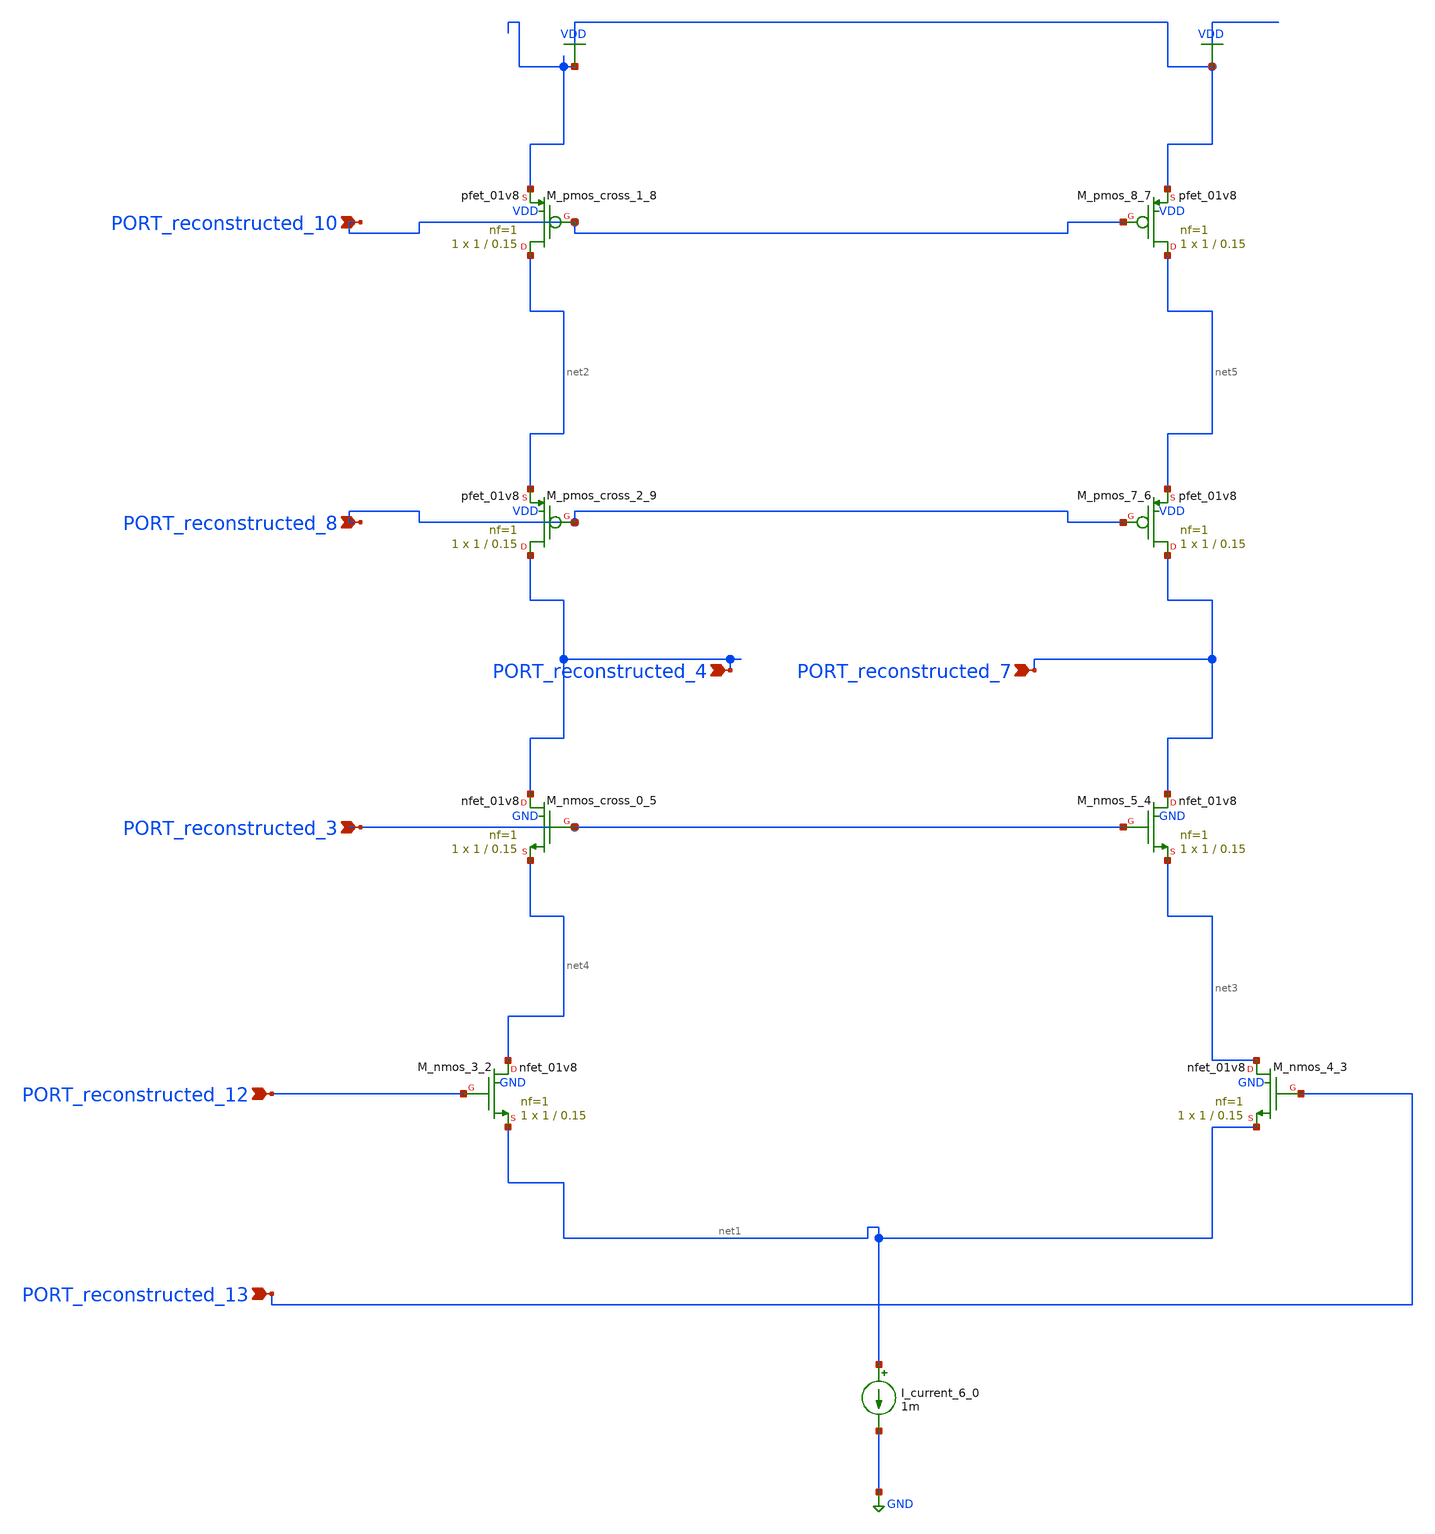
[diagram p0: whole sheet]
** sch_path: schematics/AMSNet/226.sch
**.subckt 226 PORT_reconstructed_3 PORT_reconstructed_7 PORT_reconstructed_4 PORT_reconstructed_10
*+ PORT_reconstructed_12 PORT_reconstructed_8 PORT_reconstructed_13
*.ipin PORT_reconstructed_3
*.ipin PORT_reconstructed_7
*.ipin PORT_reconstructed_4
*.ipin PORT_reconstructed_10
*.ipin PORT_reconstructed_12
*.ipin PORT_reconstructed_8
*.ipin PORT_reconstructed_13
I_current_6_0 net1 GND 1m
XM_nmos_3_2 net4 PORT_reconstructed_12 net1 GND sky130_fd_pr__nfet_01v8 L=0.15 W=1 nf=1 ad='int((1 + 1)/2) * 1 / 1 * 0.29'
+ as='int((1 + 2)/2) * 1 / 1 * 0.29' pd='2*int((1 + 1)/2) * (1 / 1 + 0.29)' ps='2*int((1 + 2)/2) * (1 / 1 + 0.29)'
+ nrd='0.29 / 1 ' nrs='0.29 / 1 ' sa=0 sb=0 sd=0 mult=1 m=1
XM_nmos_4_3 net3 PORT_reconstructed_13 net1 GND sky130_fd_pr__nfet_01v8 L=0.15 W=1 nf=1 ad='int((1 + 1)/2) * 1 / 1 * 0.29'
+ as='int((1 + 2)/2) * 1 / 1 * 0.29' pd='2*int((1 + 1)/2) * (1 / 1 + 0.29)' ps='2*int((1 + 2)/2) * (1 / 1 + 0.29)'
+ nrd='0.29 / 1 ' nrs='0.29 / 1 ' sa=0 sb=0 sd=0 mult=1 m=1
XM_nmos_5_4 PORT_reconstructed_7 PORT_reconstructed_3 net3 GND sky130_fd_pr__nfet_01v8 L=0.15 W=1 nf=1
+ ad='int((1 + 1)/2) * 1 / 1 * 0.29' as='int((1 + 2)/2) * 1 / 1 * 0.29' pd='2*int((1 + 1)/2) * (1 / 1 + 0.29)'
+ ps='2*int((1 + 2)/2) * (1 / 1 + 0.29)' nrd='0.29 / 1 ' nrs='0.29 / 1 ' sa=0 sb=0 sd=0 mult=1 m=1
XM_nmos_cross_0_5 PORT_reconstructed_4 PORT_reconstructed_3 net4 GND sky130_fd_pr__nfet_01v8 L=0.15 W=1
+ nf=1 ad='int((1 + 1)/2) * 1 / 1 * 0.29' as='int((1 + 2)/2) * 1 / 1 * 0.29' pd='2*int((1 + 1)/2) * (1 / 1 + 0.29)'
+ ps='2*int((1 + 2)/2) * (1 / 1 + 0.29)' nrd='0.29 / 1 ' nrs='0.29 / 1 ' sa=0 sb=0 sd=0 mult=1 m=1
XM_pmos_7_6 PORT_reconstructed_7 PORT_reconstructed_8 net5 VDD sky130_fd_pr__pfet_01v8 L=0.15 W=1 nf=1
+ ad='int((1 + 1)/2) * 1 / 1 * 0.29' as='int((1 + 2)/2) * 1 / 1 * 0.29' pd='2*int((1 + 1)/2) * (1 / 1 + 0.29)'
+ ps='2*int((1 + 2)/2) * (1 / 1 + 0.29)' nrd='0.29 / 1 ' nrs='0.29 / 1 ' sa=0 sb=0 sd=0 mult=1 m=1
XM_pmos_8_7 net5 PORT_reconstructed_10 VDD VDD sky130_fd_pr__pfet_01v8 L=0.15 W=1 nf=1 ad='int((1 + 1)/2) * 1 / 1 * 0.29'
+ as='int((1 + 2)/2) * 1 / 1 * 0.29' pd='2*int((1 + 1)/2) * (1 / 1 + 0.29)' ps='2*int((1 + 2)/2) * (1 / 1 + 0.29)'
+ nrd='0.29 / 1 ' nrs='0.29 / 1 ' sa=0 sb=0 sd=0 mult=1 m=1
XM_pmos_cross_1_8 net2 PORT_reconstructed_10 VDD VDD sky130_fd_pr__pfet_01v8 L=0.15 W=1 nf=1 ad='int((1 + 1)/2) * 1 / 1 * 0.29'
+ as='int((1 + 2)/2) * 1 / 1 * 0.29' pd='2*int((1 + 1)/2) * (1 / 1 + 0.29)' ps='2*int((1 + 2)/2) * (1 / 1 + 0.29)'
+ nrd='0.29 / 1 ' nrs='0.29 / 1 ' sa=0 sb=0 sd=0 mult=1 m=1
XM_pmos_cross_2_9 PORT_reconstructed_4 PORT_reconstructed_8 net2 VDD sky130_fd_pr__pfet_01v8 L=0.15 W=1
+ nf=1 ad='int((1 + 1)/2) * 1 / 1 * 0.29' as='int((1 + 2)/2) * 1 / 1 * 0.29' pd='2*int((1 + 1)/2) * (1 / 1 + 0.29)'
+ ps='2*int((1 + 2)/2) * (1 / 1 + 0.29)' nrd='0.29 / 1 ' nrs='0.29 / 1 ' sa=0 sb=0 sd=0 mult=1 m=1
**.ends
.GLOBAL GND
.GLOBAL VDD
.end
